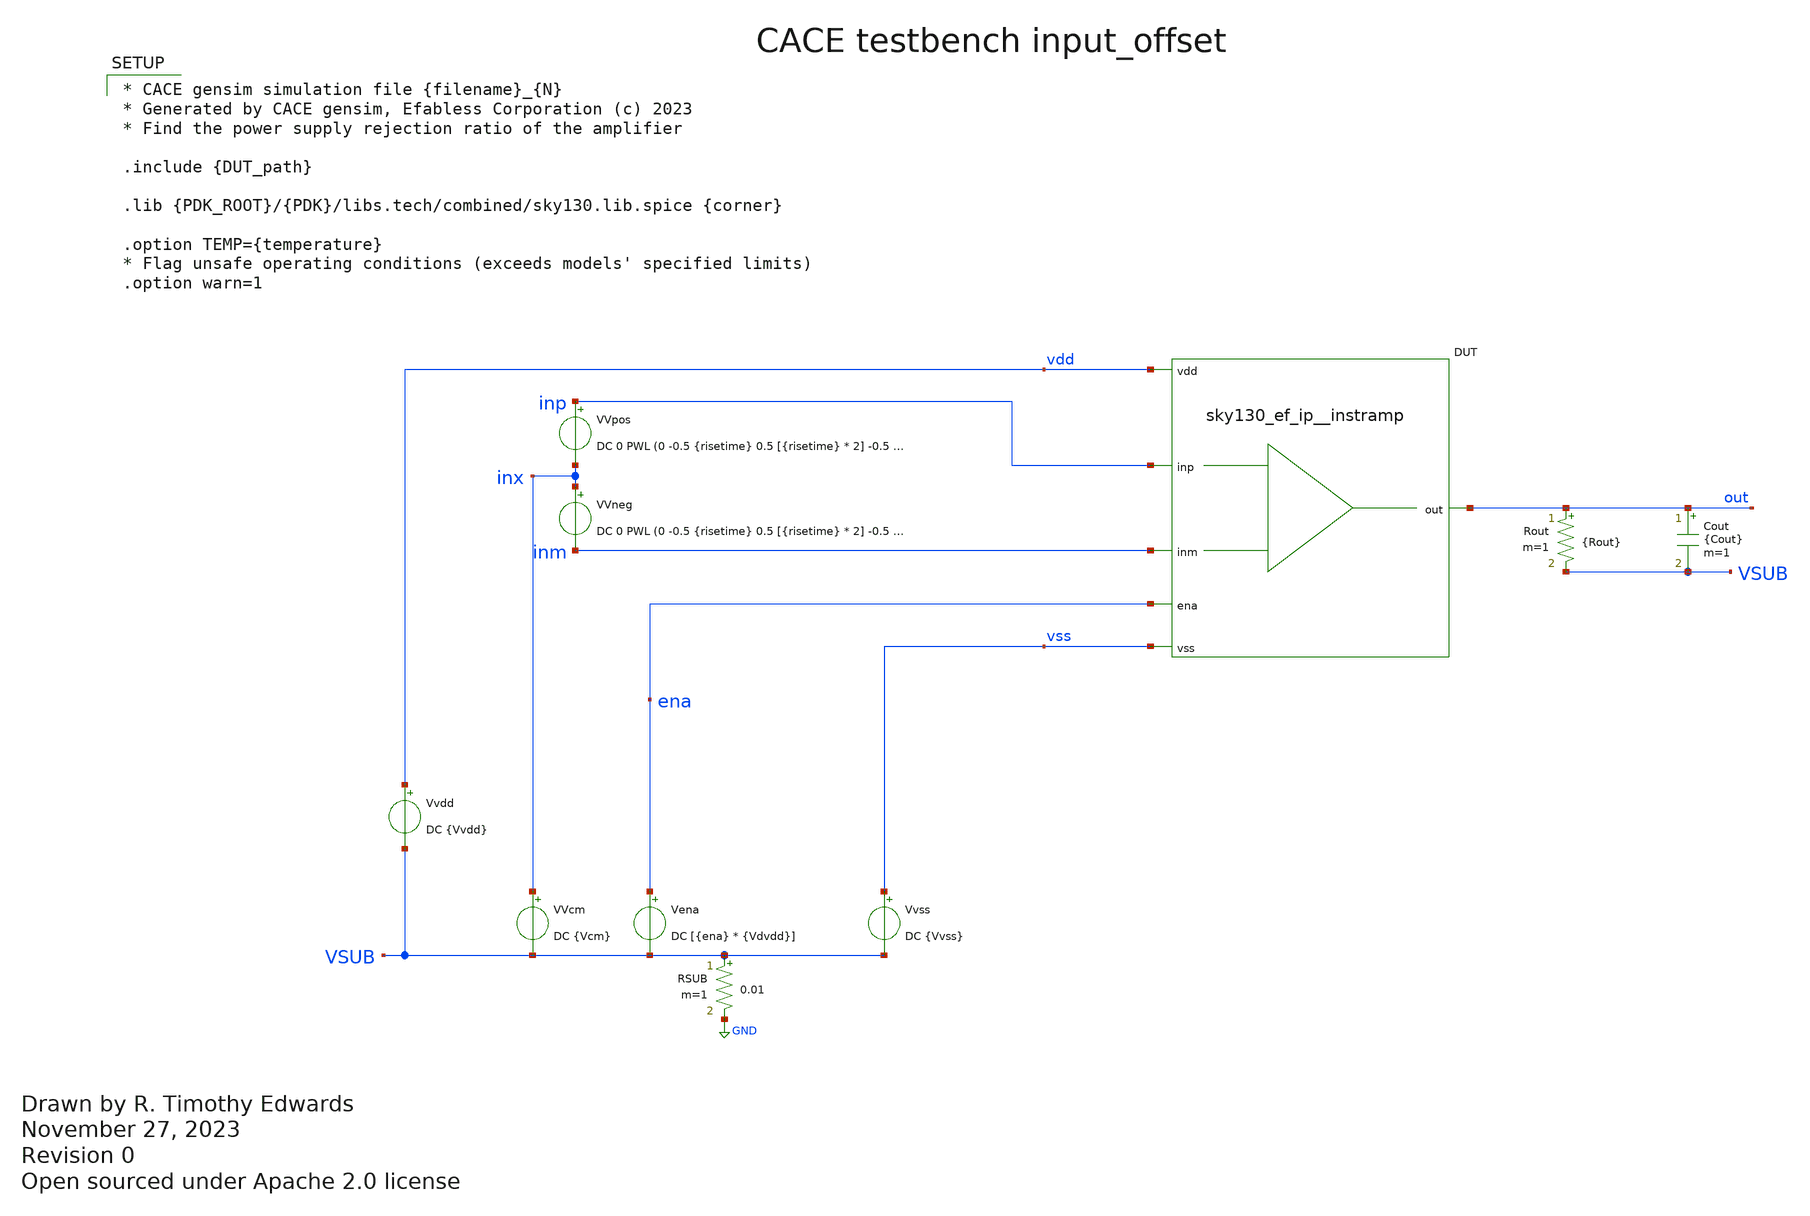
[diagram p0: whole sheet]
** sch_path: cace/input_offset.sch
* Open sourced under Apache 2.0 license
**.subckt input_offset
VVcm inx VSUB DC {Vcm}
Vena ena VSUB DC [{ena} * {Vdvdd}]
Vvss vss VSUB DC {Vvss}
Rout out VSUB {Rout} m=1
Cout out VSUB {Cout} m=1
Vvdd vdd VSUB DC {Vvdd}
RSUB VSUB GND 0.01 m=1
XDUT {PIN|vdd|vdd} {PIN|vss|vss} {PIN|inm|inm} {PIN|inp|inp} {PIN|out|out} {PIN|ena|ena} {DUT_name}
VVpos inp inx DC 0 PWL (0 -0.5 {risetime} 0.5 [{risetime} * 2] -0.5 [{risetime} * 3] 0.5 [{risetime}
+ * 4] -0.5 )
VVneg inx inm DC 0 PWL (0 -0.5 {risetime} 0.5 [{risetime} * 2] -0.5 [{risetime} * 3] 0.5 [{risetime}
+ * 4] -0.5 )
**** begin user architecture code

.control
** Find zero crossing for positive input differential, zero crossing for negative
** input differential, then compute the average
tran [{risetime} * 2 / 1000] [{risetime} * 2]
meas tran vhigh FIND V(inp) WHEN V(out) = [{Vvdd} / 2] CROSS=1
meas tran vlow FIND V(inp) WHEN V(out) = [{Vvdd} / 2] CROSS=2
let vrise = $&vhigh - {Vcm}
let vfall = $&vlow - {Vcm}

let voffset = 0.5 * ($&vrise + $&vfall)
let vhyst = $&vrise - $&vfall

echo $&voffset $&vhyst > {simpath}/{filename}_{N}.data
*set wr_singlescale
*wrdata {simpath}/{filename}_{N}.data V(out) V(inp) V(inm)
quit
.endc



* CACE gensim simulation file {filename}_{N}
* Generated by CACE gensim, Efabless Corporation (c) 2023
* Find the power supply rejection ratio of the amplifier

.include {DUT_path}

.lib {PDK_ROOT}/{PDK}/libs.tech/combined/sky130.lib.spice {corner}

.option TEMP={temperature}
* Flag unsafe operating conditions (exceeds models' specified limits)
.option warn=1


**** end user architecture code
**.ends
.GLOBAL GND
.end
